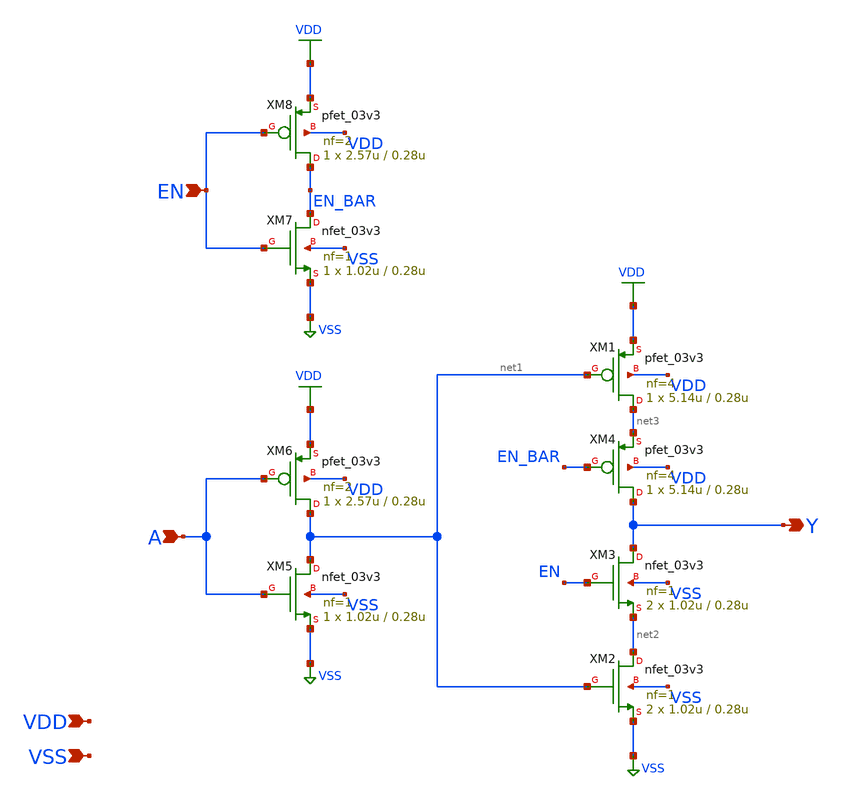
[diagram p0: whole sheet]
** sch_path: xschem/gf180mcu_ocd_sc_rt12t3v3__tbuf_2.sch
**.subckt gf180mcu_ocd_sc_rt12t3v3__tbuf_2 A EN Y VDD VSS
*.ipin A
*.ipin EN
*.opin Y
*.ipin VDD
*.ipin VSS
XM1 net3 net1 VDD VDD pfet_03v3 L=0.28u W=5.14u nf=4 ad='int((nf+1)/2) * W/nf * 0.18u' as='int((nf+2)/2) * W/nf * 0.18u'
+ pd='2*int((nf+1)/2) * (W/nf + 0.18u)' ps='2*int((nf+2)/2) * (W/nf + 0.18u)' nrd='0.18u / W' nrs='0.18u / W'
+ sa=0 sb=0 sd=0 m=1
XM2 net2 net1 VSS VSS nfet_03v3 L=0.28u W=1.02u nf=1 ad='int((nf+1)/2) * W/nf * 0.18u' as='int((nf+2)/2) * W/nf * 0.18u'
+ pd='2*int((nf+1)/2) * (W/nf + 0.18u)' ps='2*int((nf+2)/2) * (W/nf + 0.18u)' nrd='0.18u / W' nrs='0.18u / W'
+ sa=0 sb=0 sd=0 m=2
XM3 Y EN net2 VSS nfet_03v3 L=0.28u W=1.02u nf=1 ad='int((nf+1)/2) * W/nf * 0.18u' as='int((nf+2)/2) * W/nf * 0.18u'
+ pd='2*int((nf+1)/2) * (W/nf + 0.18u)' ps='2*int((nf+2)/2) * (W/nf + 0.18u)' nrd='0.18u / W' nrs='0.18u / W'
+ sa=0 sb=0 sd=0 m=2
XM4 Y EN_BAR net3 VDD pfet_03v3 L=0.28u W=5.14u nf=4 ad='int((nf+1)/2) * W/nf * 0.18u' as='int((nf+2)/2) * W/nf * 0.18u'
+ pd='2*int((nf+1)/2) * (W/nf + 0.18u)' ps='2*int((nf+2)/2) * (W/nf + 0.18u)' nrd='0.18u / W' nrs='0.18u / W'
+ sa=0 sb=0 sd=0 m=1
XM5 net1 A VSS VSS nfet_03v3 L=0.28u W=1.02u nf=1 ad='int((nf+1)/2) * W/nf * 0.18u' as='int((nf+2)/2) * W/nf * 0.18u'
+ pd='2*int((nf+1)/2) * (W/nf + 0.18u)' ps='2*int((nf+2)/2) * (W/nf + 0.18u)' nrd='0.18u / W' nrs='0.18u / W'
+ sa=0 sb=0 sd=0 m=1
XM6 net1 A VDD VDD pfet_03v3 L=0.28u W=2.57u nf=2 ad='int((nf+1)/2) * W/nf * 0.18u' as='int((nf+2)/2) * W/nf * 0.18u'
+ pd='2*int((nf+1)/2) * (W/nf + 0.18u)' ps='2*int((nf+2)/2) * (W/nf + 0.18u)' nrd='0.18u / W' nrs='0.18u / W'
+ sa=0 sb=0 sd=0 m=1
XM7 EN_BAR EN VSS VSS nfet_03v3 L=0.28u W=1.02u nf=1 ad='int((nf+1)/2) * W/nf * 0.18u' as='int((nf+2)/2) * W/nf * 0.18u'
+ pd='2*int((nf+1)/2) * (W/nf + 0.18u)' ps='2*int((nf+2)/2) * (W/nf + 0.18u)' nrd='0.18u / W' nrs='0.18u / W'
+ sa=0 sb=0 sd=0 m=1
XM8 EN_BAR EN VDD VDD pfet_03v3 L=0.28u W=2.57u nf=2 ad='int((nf+1)/2) * W/nf * 0.18u' as='int((nf+2)/2) * W/nf * 0.18u'
+ pd='2*int((nf+1)/2) * (W/nf + 0.18u)' ps='2*int((nf+2)/2) * (W/nf + 0.18u)' nrd='0.18u / W' nrs='0.18u / W'
+ sa=0 sb=0 sd=0 m=1
**.ends
.GLOBAL VDD
.GLOBAL VSS
.end
